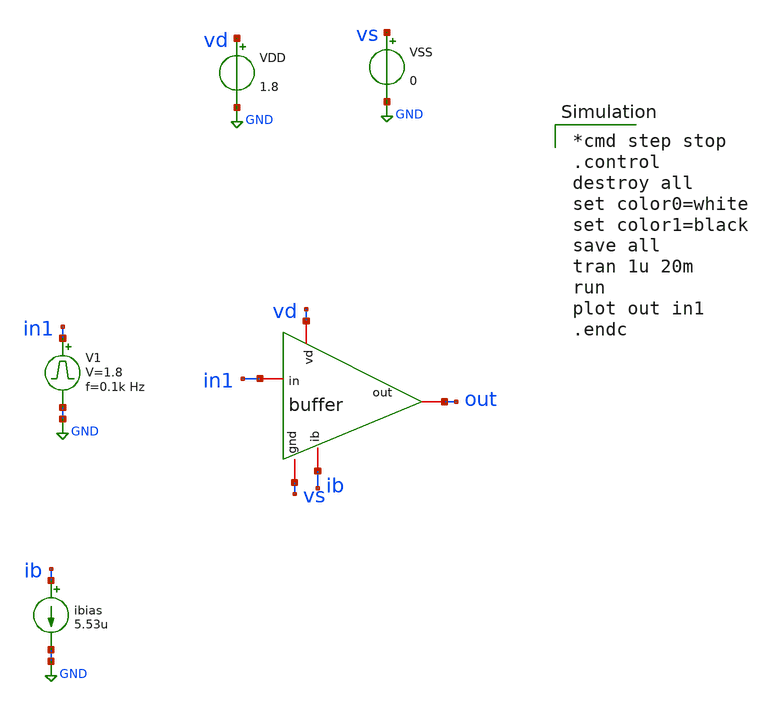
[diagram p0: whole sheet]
** sch_path: buffer/xschem/buffer_tb-largesignal.sch
* Copyright 2020 Stefan Frederik Schippers
* Licensed under the Apache License, Version 2.0 (the "License");
* you may not use this file except in compliance with the License.
* You may obtain a copy of the License at
* https://www.apache.org/licenses/LICENSE-2.0
* Unless required by applicable law or agreed to in writing, software
* distributed under the License is distributed on an "AS IS" BASIS,
* WITHOUT WARRANTIES OR CONDITIONS OF ANY KIND, either express or implied.
* See the License for the specific language governing permissions and
* limitations under the License.
**.subckt buffer_tb-largesignal
ibias ib GND 5.53u
VDD vd GND 1.8
VSS vs GND 0
V1 in1 GND pulse 0 1.8 '0.495/ 0.1k ' '0.01/0.1k ' '0.01/0.1k ' '0.49/0.1k ' '1/0.1k '
X1 vd in1 out ib vs buffer
**** begin user architecture code

*cmd step stop
.control
destroy all
set color0=white
set color1=black
save all
tran 1u 20m
run
plot out in1
.endc

 .lib $::SKYWATER_MODELS/sky130.lib.spice tt
.include $::SKYWATER_STDCELLS/sky130_fd_sc_hd.spice

**** end user architecture code
**.ends

* expanding   symbol:  /home/hugodg/projects-sky130/temp-sensor/amp-op/xschem/buffer.sym # of pins=5
** sym_path: buffer/xschem/buffer.sym
** sch_path: buffer/xschem/buffer.sch
.subckt buffer vd in out ib gnd
*.iopin vd
*.iopin ib
*.iopin out
*.iopin in
*.iopin gnd
XM3 net2 net2 vd vd sky130_fd_pr__pfet_01v8 L=1 W=1 nf=1 ad='int((nf+1)/2) * W/nf * 0.29' as='int((nf+2)/2) * W/nf * 0.29'
+ pd='2*int((nf+1)/2) * (W/nf + 0.29)' ps='2*int((nf+2)/2) * (W/nf + 0.29)' nrd='0.29 / W' nrs='0.29 / W'
+ sa=0 sb=0 sd=0 mult=1 m=1
XM1 net2 out net4 gnd sky130_fd_pr__nfet_01v8 L=1 W=10 nf=10 ad='int((nf+1)/2) * W/nf * 0.29' as='int((nf+2)/2) * W/nf * 0.29'
+ pd='2*int((nf+1)/2) * (W/nf + 0.29)' ps='2*int((nf+2)/2) * (W/nf + 0.29)' nrd='0.29 / W' nrs='0.29 / W'
+ sa=0 sb=0 sd=0 mult=1 m=1
XM2 net3 in net4 gnd sky130_fd_pr__nfet_01v8 L=1 W=10 nf=10 ad='int((nf+1)/2) * W/nf * 0.29' as='int((nf+2)/2) * W/nf * 0.29'
+ pd='2*int((nf+1)/2) * (W/nf + 0.29)' ps='2*int((nf+2)/2) * (W/nf + 0.29)' nrd='0.29 / W' nrs='0.29 / W'
+ sa=0 sb=0 sd=0 mult=1 m=1
XM4 net3 net3 vd vd sky130_fd_pr__pfet_01v8 L=1 W=1 nf=1 ad='int((nf+1)/2) * W/nf * 0.29' as='int((nf+2)/2) * W/nf * 0.29'
+ pd='2*int((nf+1)/2) * (W/nf + 0.29)' ps='2*int((nf+2)/2) * (W/nf + 0.29)' nrd='0.29 / W' nrs='0.29 / W'
+ sa=0 sb=0 sd=0 mult=1 m=1
XM5 net4 ib gnd gnd sky130_fd_pr__nfet_01v8 L=1 W=1 nf=1 ad='int((nf+1)/2) * W/nf * 0.29' as='int((nf+2)/2) * W/nf * 0.29'
+ pd='2*int((nf+1)/2) * (W/nf + 0.29)' ps='2*int((nf+2)/2) * (W/nf + 0.29)' nrd='0.29 / W' nrs='0.29 / W'
+ sa=0 sb=0 sd=0 mult=1 m=1
XM6 out net3 vd vd sky130_fd_pr__pfet_01v8 L=1 W=10 nf=10 ad='int((nf+1)/2) * W/nf * 0.29' as='int((nf+2)/2) * W/nf * 0.29'
+ pd='2*int((nf+1)/2) * (W/nf + 0.29)' ps='2*int((nf+2)/2) * (W/nf + 0.29)' nrd='0.29 / W' nrs='0.29 / W'
+ sa=0 sb=0 sd=0 mult=1 m=1
XM7 out net1 gnd gnd sky130_fd_pr__nfet_01v8 L=1 W=10 nf=10 ad='int((nf+1)/2) * W/nf * 0.29' as='int((nf+2)/2) * W/nf * 0.29'
+ pd='2*int((nf+1)/2) * (W/nf + 0.29)' ps='2*int((nf+2)/2) * (W/nf + 0.29)' nrd='0.29 / W' nrs='0.29 / W'
+ sa=0 sb=0 sd=0 mult=1 m=1
XM8 net1 net2 vd vd sky130_fd_pr__pfet_01v8 L=1 W=10 nf=10 ad='int((nf+1)/2) * W/nf * 0.29' as='int((nf+2)/2) * W/nf * 0.29'
+ pd='2*int((nf+1)/2) * (W/nf + 0.29)' ps='2*int((nf+2)/2) * (W/nf + 0.29)' nrd='0.29 / W' nrs='0.29 / W'
+ sa=0 sb=0 sd=0 mult=1 m=1
XM9 net1 net1 gnd gnd sky130_fd_pr__nfet_01v8 L=1 W=10 nf=10 ad='int((nf+1)/2) * W/nf * 0.29' as='int((nf+2)/2) * W/nf * 0.29'
+ pd='2*int((nf+1)/2) * (W/nf + 0.29)' ps='2*int((nf+2)/2) * (W/nf + 0.29)' nrd='0.29 / W' nrs='0.29 / W'
+ sa=0 sb=0 sd=0 mult=1 m=1
XM10 ib ib gnd gnd sky130_fd_pr__nfet_01v8 L=1 W=1 nf=1 ad='int((nf+1)/2) * W/nf * 0.29' as='int((nf+2)/2) * W/nf * 0.29'
+ pd='2*int((nf+1)/2) * (W/nf + 0.29)' ps='2*int((nf+2)/2) * (W/nf + 0.29)' nrd='0.29 / W' nrs='0.29 / W'
+ sa=0 sb=0 sd=0 mult=1 m=1
.ends

.GLOBAL GND
.end
